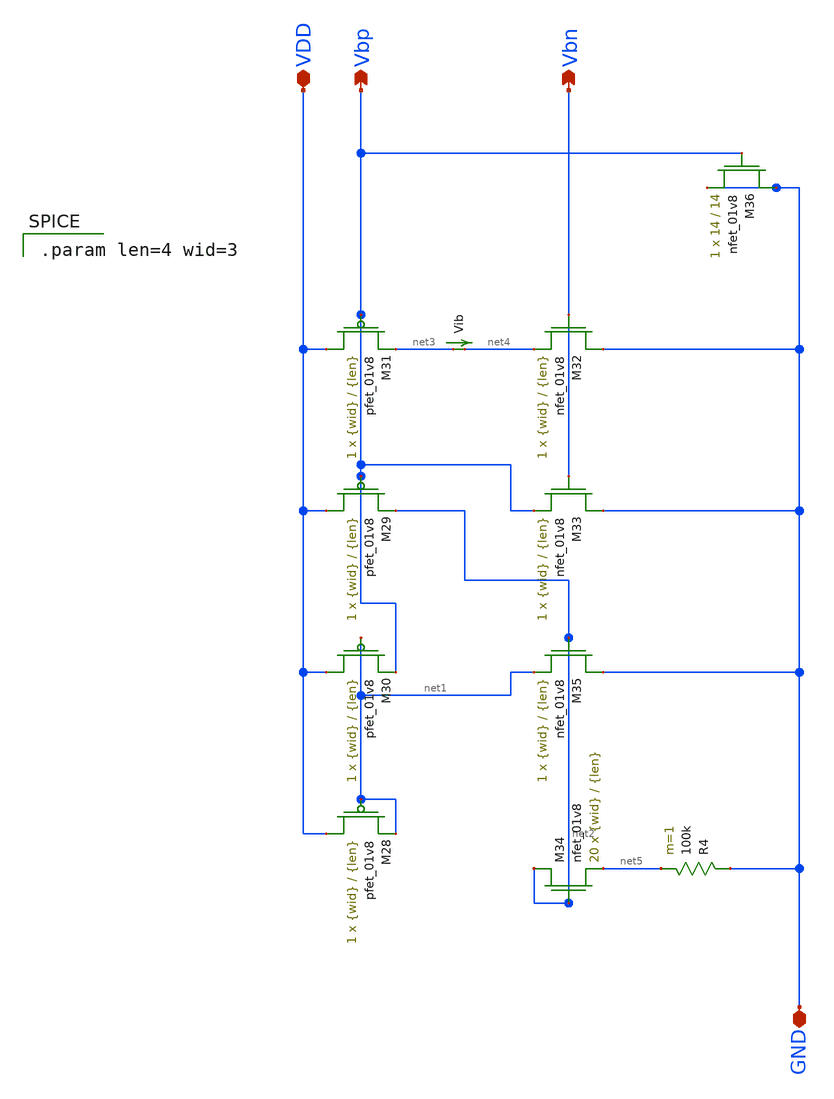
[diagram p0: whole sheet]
** sch_path: mp3/Layout_Schem_Designs/bias_gen_lds.sch
**.subckt bias_gen_lds Vbp VDD Vbn GND
*.opin Vbp
*.iopin VDD
*.opin Vbn
*.iopin GND
XM28 VDD net1 net1 VDD sky130_fd_pr__pfet_01v8 L={len} W={wid} nf=1 ad='int((nf+1)/2) * W/nf * 0.29'
+ as='int((nf+2)/2) * W/nf * 0.29' pd='2*int((nf+1)/2) * (W/nf + 0.29)' ps='2*int((nf+2)/2) * (W/nf + 0.29)'
+ nrd='0.29 / W' nrs='0.29 / W' sa=0 sb=0 sd=0 mult=1 m=1
XM29 VDD Vbp net2 VDD sky130_fd_pr__pfet_01v8 L={len} W={wid} nf=1 ad='int((nf+1)/2) * W/nf * 0.29' as='int((nf+2)/2) * W/nf * 0.29'
+ pd='2*int((nf+1)/2) * (W/nf + 0.29)' ps='2*int((nf+2)/2) * (W/nf + 0.29)' nrd='0.29 / W' nrs='0.29 / W'
+ sa=0 sb=0 sd=0 mult=1 m=1
XM30 VDD net1 Vbp VDD sky130_fd_pr__pfet_01v8 L={len} W={wid} nf=1 ad='int((nf+1)/2) * W/nf * 0.29' as='int((nf+2)/2) * W/nf * 0.29'
+ pd='2*int((nf+1)/2) * (W/nf + 0.29)' ps='2*int((nf+2)/2) * (W/nf + 0.29)' nrd='0.29 / W' nrs='0.29 / W'
+ sa=0 sb=0 sd=0 mult=1 m=1
XM31 VDD Vbp net3 VDD sky130_fd_pr__pfet_01v8 L={len} W={wid} nf=1 ad='int((nf+1)/2) * W/nf * 0.29' as='int((nf+2)/2) * W/nf * 0.29'
+ pd='2*int((nf+1)/2) * (W/nf + 0.29)' ps='2*int((nf+2)/2) * (W/nf + 0.29)' nrd='0.29 / W' nrs='0.29 / W'
+ sa=0 sb=0 sd=0 mult=1 m=1
XM32 GND Vbn net4 GND sky130_fd_pr__nfet_01v8 L={len} W={wid} nf=1 ad='int((nf+1)/2) * W/nf * 0.29' as='int((nf+2)/2) * W/nf * 0.29'
+ pd='2*int((nf+1)/2) * (W/nf + 0.29)' ps='2*int((nf+2)/2) * (W/nf + 0.29)' nrd='0.29 / W' nrs='0.29 / W'
+ sa=0 sb=0 sd=0 mult=1 m=1
XM33 GND Vbn Vbp GND sky130_fd_pr__nfet_01v8 L={len} W={wid} nf=1 ad='int((nf+1)/2) * W/nf * 0.29' as='int((nf+2)/2) * W/nf * 0.29'
+ pd='2*int((nf+1)/2) * (W/nf + 0.29)' ps='2*int((nf+2)/2) * (W/nf + 0.29)' nrd='0.29 / W' nrs='0.29 / W'
+ sa=0 sb=0 sd=0 mult=1 m=1
Vib net3 net4 0
.save i(vib)
XM34 net2 net2 net5 GND sky130_fd_pr__nfet_01v8 L={len} W={wid} nf=1 ad='int((nf+1)/2) * W/nf * 0.29'
+ as='int((nf+2)/2) * W/nf * 0.29' pd='2*int((nf+1)/2) * (W/nf + 0.29)' ps='2*int((nf+2)/2) * (W/nf + 0.29)'
+ nrd='0.29 / W' nrs='0.29 / W' sa=0 sb=0 sd=0 mult=20 m=20
XM35 GND net2 net1 GND sky130_fd_pr__nfet_01v8 L={len} W={wid} nf=1 ad='int((nf+1)/2) * W/nf * 0.29'
+ as='int((nf+2)/2) * W/nf * 0.29' pd='2*int((nf+1)/2) * (W/nf + 0.29)' ps='2*int((nf+2)/2) * (W/nf + 0.29)'
+ nrd='0.29 / W' nrs='0.29 / W' sa=0 sb=0 sd=0 mult=1 m=1
R4 GND net5 100k m=1
XM36 GND Vbp GND GND sky130_fd_pr__nfet_01v8 L=14 W=14 nf=1 ad='int((nf+1)/2) * W/nf * 0.29' as='int((nf+2)/2) * W/nf * 0.29'
+ pd='2*int((nf+1)/2) * (W/nf + 0.29)' ps='2*int((nf+2)/2) * (W/nf + 0.29)' nrd='0.29 / W' nrs='0.29 / W'
+ sa=0 sb=0 sd=0 mult=1 m=1
**** begin user architecture code

.param len=4 wid=3

**** end user architecture code
**.ends
.end
